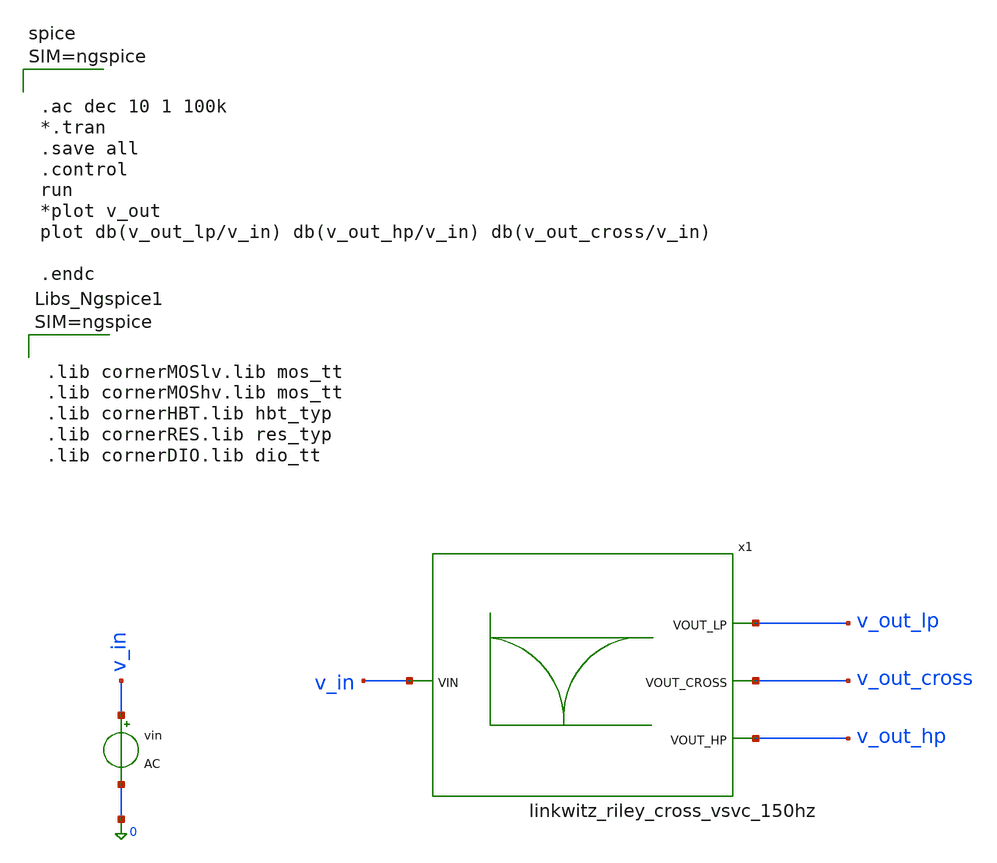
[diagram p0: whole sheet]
** sch_path: 003_Ideal_Circuits/linkwitz_riley_top_tb.sch
**.subckt linkwitz_riley_top_tb
vin v_in 0 AC
x1 v_out_lp v_out_cross v_in v_out_hp linkwitz_riley_cross_vsvc_150hz
**** begin user architecture code



.lib cornerMOSlv.lib mos_tt
.lib cornerMOShv.lib mos_tt
.lib cornerHBT.lib hbt_typ
.lib cornerRES.lib res_typ
.lib cornerDIO.lib dio_tt






.ac dec 10 1 100k
*.tran
.save all
.control
run
*plot v_out
plot db(v_out_lp/v_in) db(v_out_hp/v_in) db(v_out_cross/v_in)

.endc



**** end user architecture code
**.ends

* expanding   symbol:  003_Ideal_Circuits/linkwitz_riley_cross_vsvc_150hz.sym # of pins=4
** sym_path: 003_Ideal_Circuits/linkwitz_riley_cross_vsvc_150hz.sym
** sch_path: 003_Ideal_Circuits/linkwitz_riley_cross_vsvc_150hz.sch
.subckt linkwitz_riley_cross_vsvc_150hz VOUT_LP VOUT_CROSS VIN VOUT_HP
*.ipin VIN
*.opin VOUT_LP
*.opin VOUT_HP
*.opin VOUT_CROSS
R1 net1 VIN R_LP m=1
R2 net2 net1 R_LP m=1
C1 net1 VOUT_LP C_LP m=1
C2 net2 0 C_LP m=1
.param C_LP=21.221e-9
.param R_LP=50k
R3 0 net4 R_HP m=1
R4 net3 VOUT_HP R_HP m=1
C3 net3 net4 C_HP m=1
C4 VIN net3 C_HP m=1
.param C_HP=50e-9
.param R_HP=21.221k
R5 net6 net5 R_IN m=1
R6 VOUT_HP net6 R_IN m=1
.param R_IN=1k
R7 net7 VOUT_CROSS R_IN m=1
R8 net5 net7 R_IN m=1
R9 VOUT_LP net7 R_IN m=1
E2 VOUT_LP 0 net2 VOUT_LP 1e6
E1 VOUT_HP 0 net4 VOUT_HP 1e6
E3 net5 0 0 net6 1e6
E4 VOUT_CROSS 0 0 net7 1e6
.ends

.end
